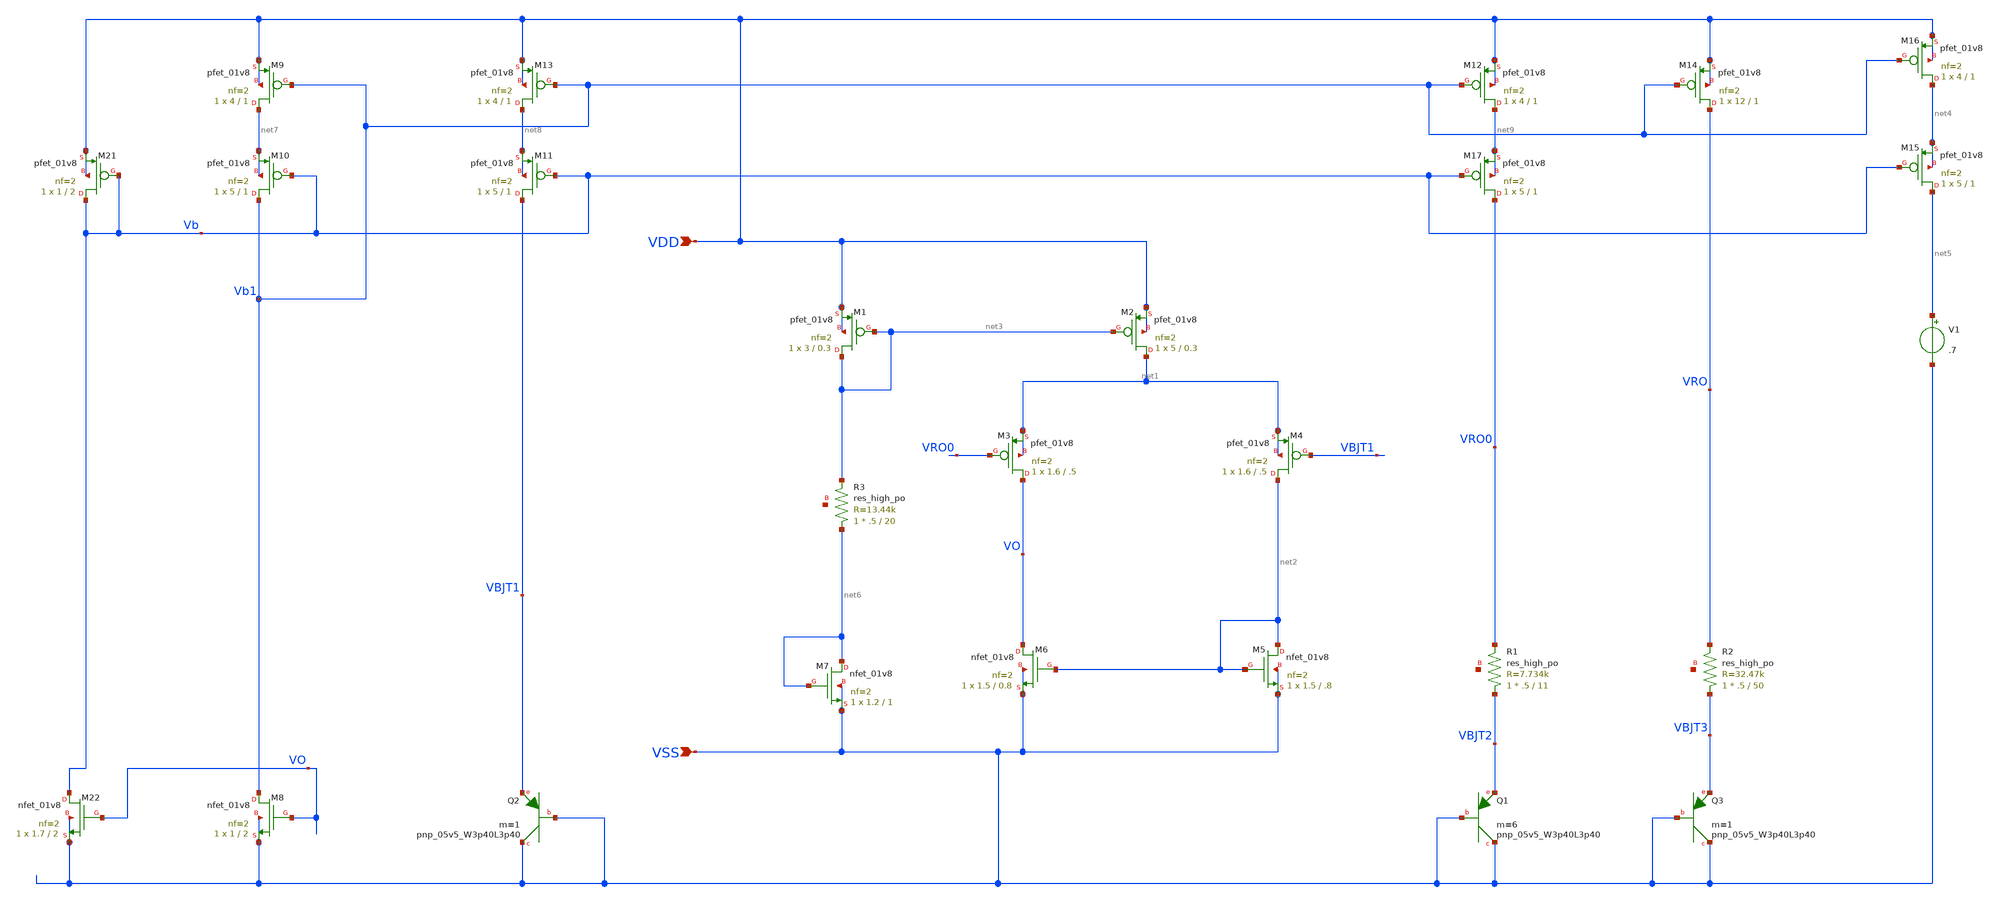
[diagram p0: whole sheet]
** sch_path: design/CNR_GR02_SKY130NM/CNR_GR02.sch
**.subckt CNR_GR02 VDD VSS
*.ipin VDD
*.ipin VSS
XQ1 VSS VSS VBJT2 sky130_fd_pr__pnp_05v5_W3p40L3p40 m=6
XQ2 VSS VSS VBJT1 sky130_fd_pr__pnp_05v5_W3p40L3p40 m=1
XM12 net9 Vb1 VDD VDD sky130_fd_pr__pfet_01v8 L=1 W=4 nf=2 ad='int((nf+1)/2) * W/nf * 0.29' as='int((nf+2)/2) * W/nf * 0.29'
+ pd='2*int((nf+1)/2) * (W/nf + 0.29)' ps='2*int((nf+2)/2) * (W/nf + 0.29)' nrd='0.29 / W' nrs='0.29 / W'
+ sa=0 sb=0 sd=0 mult=1 m=1
XM13 net8 Vb1 VDD VDD sky130_fd_pr__pfet_01v8 L=1 W=4 nf=2 ad='int((nf+1)/2) * W/nf * 0.29' as='int((nf+2)/2) * W/nf * 0.29'
+ pd='2*int((nf+1)/2) * (W/nf + 0.29)' ps='2*int((nf+2)/2) * (W/nf + 0.29)' nrd='0.29 / W' nrs='0.29 / W'
+ sa=0 sb=0 sd=0 mult=1 m=1
XM14 VRO Vb1 VDD VDD sky130_fd_pr__pfet_01v8 L=1 W=12 nf=2 ad='int((nf+1)/2) * W/nf * 0.29' as='int((nf+2)/2) * W/nf * 0.29'
+ pd='2*int((nf+1)/2) * (W/nf + 0.29)' ps='2*int((nf+2)/2) * (W/nf + 0.29)' nrd='0.29 / W' nrs='0.29 / W'
+ sa=0 sb=0 sd=0 mult=1 m=1
XQ3 VSS VSS VBJT3 sky130_fd_pr__pnp_05v5_W3p40L3p40 m=1
V1 net5 VSS .7
.save i(v1)
XM16 net4 Vb1 VDD VDD sky130_fd_pr__pfet_01v8 L=1 W=4 nf=2 ad='int((nf+1)/2) * W/nf * 0.29' as='int((nf+2)/2) * W/nf * 0.29'
+ pd='2*int((nf+1)/2) * (W/nf + 0.29)' ps='2*int((nf+2)/2) * (W/nf + 0.29)' nrd='0.29 / W' nrs='0.29 / W'
+ sa=0 sb=0 sd=0 mult=1 m=1
XM1 net3 net3 VDD VDD sky130_fd_pr__pfet_01v8 L=0.3 W=3 nf=2 ad='int((nf+1)/2) * W/nf * 0.29' as='int((nf+2)/2) * W/nf * 0.29'
+ pd='2*int((nf+1)/2) * (W/nf + 0.29)' ps='2*int((nf+2)/2) * (W/nf + 0.29)' nrd='0.29 / W' nrs='0.29 / W'
+ sa=0 sb=0 sd=0 mult=1 m=1
XM2 net1 net3 VDD VDD sky130_fd_pr__pfet_01v8 L=0.3 W=5 nf=2 ad='int((nf+1)/2) * W/nf * 0.29' as='int((nf+2)/2) * W/nf * 0.29'
+ pd='2*int((nf+1)/2) * (W/nf + 0.29)' ps='2*int((nf+2)/2) * (W/nf + 0.29)' nrd='0.29 / W' nrs='0.29 / W'
+ sa=0 sb=0 sd=0 mult=1 m=1
XM3 VO VRO0 net1 net1 sky130_fd_pr__pfet_01v8 L=.5 W=1.6 nf=2 ad='int((nf+1)/2) * W/nf * 0.29' as='int((nf+2)/2) * W/nf * 0.29'
+ pd='2*int((nf+1)/2) * (W/nf + 0.29)' ps='2*int((nf+2)/2) * (W/nf + 0.29)' nrd='0.29 / W' nrs='0.29 / W'
+ sa=0 sb=0 sd=0 mult=1 m=1
XM4 net2 VBJT1 net1 net1 sky130_fd_pr__pfet_01v8 L=.5 W=1.6 nf=2 ad='int((nf+1)/2) * W/nf * 0.29' as='int((nf+2)/2) * W/nf * 0.29'
+ pd='2*int((nf+1)/2) * (W/nf + 0.29)' ps='2*int((nf+2)/2) * (W/nf + 0.29)' nrd='0.29 / W' nrs='0.29 / W'
+ sa=0 sb=0 sd=0 mult=1 m=1
XM5 net2 net2 VSS VSS sky130_fd_pr__nfet_01v8 L=.8 W=1.5 nf=2 ad='int((nf+1)/2) * W/nf * 0.29' as='int((nf+2)/2) * W/nf * 0.29'
+ pd='2*int((nf+1)/2) * (W/nf + 0.29)' ps='2*int((nf+2)/2) * (W/nf + 0.29)' nrd='0.29 / W' nrs='0.29 / W'
+ sa=0 sb=0 sd=0 mult=1 m=1
XM6 VO net2 VSS VSS sky130_fd_pr__nfet_01v8 L=0.8 W=1.5 nf=2 ad='int((nf+1)/2) * W/nf * 0.29' as='int((nf+2)/2) * W/nf * 0.29'
+ pd='2*int((nf+1)/2) * (W/nf + 0.29)' ps='2*int((nf+2)/2) * (W/nf + 0.29)' nrd='0.29 / W' nrs='0.29 / W'
+ sa=0 sb=0 sd=0 mult=1 m=1
XM15 net5 Vb net4 net4 sky130_fd_pr__pfet_01v8 L=1 W=5 nf=2 ad='int((nf+1)/2) * W/nf * 0.29' as='int((nf+2)/2) * W/nf * 0.29'
+ pd='2*int((nf+1)/2) * (W/nf + 0.29)' ps='2*int((nf+2)/2) * (W/nf + 0.29)' nrd='0.29 / W' nrs='0.29 / W'
+ sa=0 sb=0 sd=0 mult=1 m=1
XR2 VBJT3 VRO net10 sky130_fd_pr__res_high_po W=.5 L=50 mult=1 m=1
XR1 VBJT2 VRO0 net11 sky130_fd_pr__res_high_po W=.5 L=11 mult=1 m=1
XM7 net6 net6 VSS VSS sky130_fd_pr__nfet_01v8 L=1 W=1.2 nf=2 ad='int((nf+1)/2) * W/nf * 0.29' as='int((nf+2)/2) * W/nf * 0.29'
+ pd='2*int((nf+1)/2) * (W/nf + 0.29)' ps='2*int((nf+2)/2) * (W/nf + 0.29)' nrd='0.29 / W' nrs='0.29 / W'
+ sa=0 sb=0 sd=0 mult=1 m=1
XR3 net6 net3 net12 sky130_fd_pr__res_high_po W=.5 L=20 mult=1 m=1
XM8 Vb1 VO VSS VSS sky130_fd_pr__nfet_01v8 L=2 W=1 nf=2 ad='int((nf+1)/2) * W/nf * 0.29' as='int((nf+2)/2) * W/nf * 0.29'
+ pd='2*int((nf+1)/2) * (W/nf + 0.29)' ps='2*int((nf+2)/2) * (W/nf + 0.29)' nrd='0.29 / W' nrs='0.29 / W'
+ sa=0 sb=0 sd=0 mult=1 m=1
XM9 net7 Vb1 VDD VDD sky130_fd_pr__pfet_01v8 L=1 W=4 nf=2 ad='int((nf+1)/2) * W/nf * 0.29' as='int((nf+2)/2) * W/nf * 0.29'
+ pd='2*int((nf+1)/2) * (W/nf + 0.29)' ps='2*int((nf+2)/2) * (W/nf + 0.29)' nrd='0.29 / W' nrs='0.29 / W'
+ sa=0 sb=0 sd=0 mult=1 m=1
XM10 Vb1 Vb net7 net7 sky130_fd_pr__pfet_01v8 L=1 W=5 nf=2 ad='int((nf+1)/2) * W/nf * 0.29' as='int((nf+2)/2) * W/nf * 0.29'
+ pd='2*int((nf+1)/2) * (W/nf + 0.29)' ps='2*int((nf+2)/2) * (W/nf + 0.29)' nrd='0.29 / W' nrs='0.29 / W'
+ sa=0 sb=0 sd=0 mult=1 m=1
XM11 VBJT1 Vb net8 net8 sky130_fd_pr__pfet_01v8 L=1 W=5 nf=2 ad='int((nf+1)/2) * W/nf * 0.29' as='int((nf+2)/2) * W/nf * 0.29'
+ pd='2*int((nf+1)/2) * (W/nf + 0.29)' ps='2*int((nf+2)/2) * (W/nf + 0.29)' nrd='0.29 / W' nrs='0.29 / W'
+ sa=0 sb=0 sd=0 mult=1 m=1
XM17 VRO0 Vb net9 net9 sky130_fd_pr__pfet_01v8 L=1 W=5 nf=2 ad='int((nf+1)/2) * W/nf * 0.29' as='int((nf+2)/2) * W/nf * 0.29'
+ pd='2*int((nf+1)/2) * (W/nf + 0.29)' ps='2*int((nf+2)/2) * (W/nf + 0.29)' nrd='0.29 / W' nrs='0.29 / W'
+ sa=0 sb=0 sd=0 mult=1 m=1
XM21 Vb Vb VDD VDD sky130_fd_pr__pfet_01v8 L=2 W=1 nf=2 ad='int((nf+1)/2) * W/nf * 0.29' as='int((nf+2)/2) * W/nf * 0.29'
+ pd='2*int((nf+1)/2) * (W/nf + 0.29)' ps='2*int((nf+2)/2) * (W/nf + 0.29)' nrd='0.29 / W' nrs='0.29 / W'
+ sa=0 sb=0 sd=0 mult=1 m=1
XM22 Vb VO VSS VSS sky130_fd_pr__nfet_01v8 L=2 W=1.7 nf=2 ad='int((nf+1)/2) * W/nf * 0.29' as='int((nf+2)/2) * W/nf * 0.29'
+ pd='2*int((nf+1)/2) * (W/nf + 0.29)' ps='2*int((nf+2)/2) * (W/nf + 0.29)' nrd='0.29 / W' nrs='0.29 / W'
+ sa=0 sb=0 sd=0 mult=1 m=1
**.ends
.end
